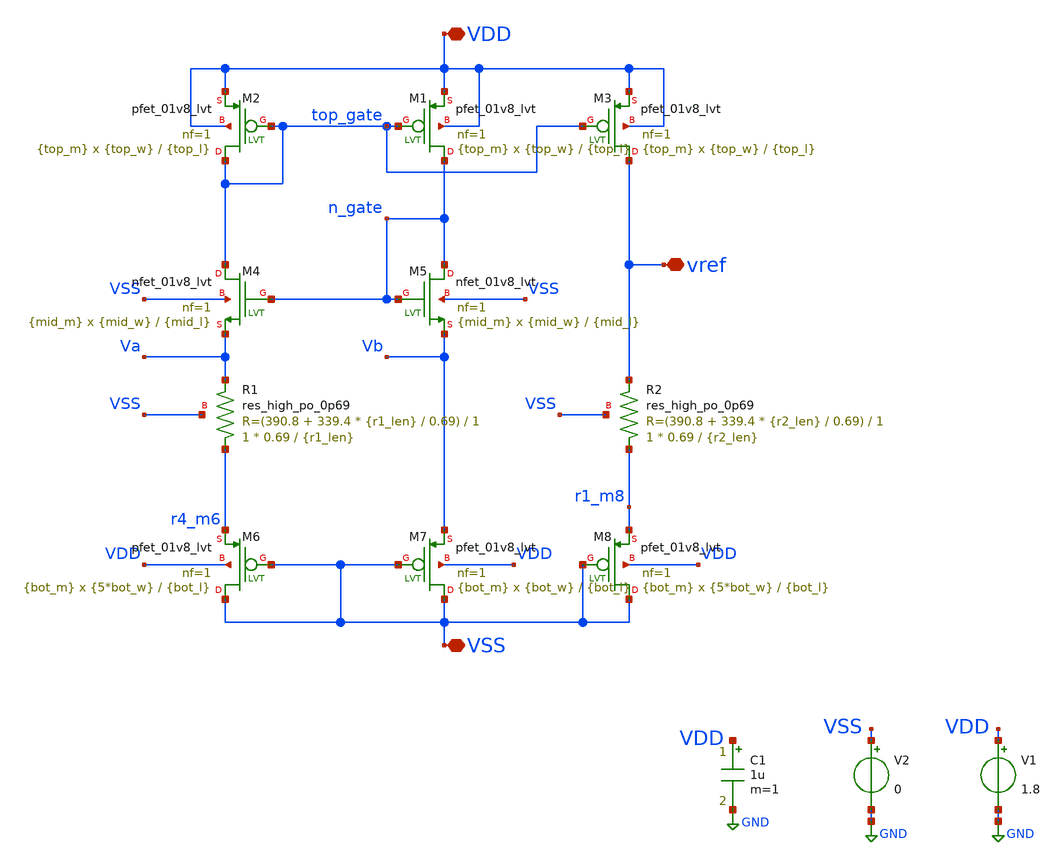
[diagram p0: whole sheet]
** sch_path: xschem/bandgap-op.sch
**.subckt bandgap-op VSS VDD vref
*.iopin VSS
*.iopin VDD
*.iopin vref
XR1 r4_m6 Va VSS sky130_fd_pr__res_high_po_0p69 L={r1_len} mult=1 m=1
XR2 r1_m8 vref VSS sky130_fd_pr__res_high_po_0p69 L={r2_len} mult=1 m=1
V1 VDD GND 1.8
V2 VSS GND 0
C1 VDD GND 1u m=1
XM5 n_gate n_gate Vb VSS sky130_fd_pr__nfet_01v8_lvt L={mid_l} W={mid_w} nf=1 ad='int((nf+1)/2) * W/nf * 0.29'
+ as='int((nf+2)/2) * W/nf * 0.29' pd='2*int((nf+1)/2) * (W/nf + 0.29)' ps='2*int((nf+2)/2) * (W/nf + 0.29)'
+ nrd='0.29 / W' nrs='0.29 / W' sa=0 sb=0 sd=0 mult={mid_m} m={mid_m}
XM3 vref top_gate VDD VDD sky130_fd_pr__pfet_01v8_lvt L={top_l} W={top_w} nf=1 ad='int((nf+1)/2) * W/nf * 0.29'
+ as='int((nf+2)/2) * W/nf * 0.29' pd='2*int((nf+1)/2) * (W/nf + 0.29)' ps='2*int((nf+2)/2) * (W/nf + 0.29)'
+ nrd='0.29 / W' nrs='0.29 / W' sa=0 sb=0 sd=0 mult={top_m} m={top_m}
XM1 n_gate top_gate VDD VDD sky130_fd_pr__pfet_01v8_lvt L={top_l} W={top_w} nf=1 ad='int((nf+1)/2) * W/nf * 0.29'
+ as='int((nf+2)/2) * W/nf * 0.29' pd='2*int((nf+1)/2) * (W/nf + 0.29)' ps='2*int((nf+2)/2) * (W/nf + 0.29)'
+ nrd='0.29 / W' nrs='0.29 / W' sa=0 sb=0 sd=0 mult={top_m} m={top_m}
XM2 top_gate top_gate VDD VDD sky130_fd_pr__pfet_01v8_lvt L={top_l} W={top_w} nf=1 ad='int((nf+1)/2) * W/nf * 0.29'
+ as='int((nf+2)/2) * W/nf * 0.29' pd='2*int((nf+1)/2) * (W/nf + 0.29)' ps='2*int((nf+2)/2) * (W/nf + 0.29)'
+ nrd='0.29 / W' nrs='0.29 / W' sa=0 sb=0 sd=0 mult={top_m} m={top_m}
XM4 top_gate n_gate Va VSS sky130_fd_pr__nfet_01v8_lvt L={mid_l} W={mid_w} nf=1 ad='int((nf+1)/2) * W/nf * 0.29'
+ as='int((nf+2)/2) * W/nf * 0.29' pd='2*int((nf+1)/2) * (W/nf + 0.29)' ps='2*int((nf+2)/2) * (W/nf + 0.29)'
+ nrd='0.29 / W' nrs='0.29 / W' sa=0 sb=0 sd=0 mult={mid_m} m={mid_m}
XM6 VSS VSS r4_m6 VDD sky130_fd_pr__pfet_01v8_lvt L={bot_l} W={5*bot_w} nf=1 ad='int((nf+1)/2) * W/nf * 0.29'
+ as='int((nf+2)/2) * W/nf * 0.29' pd='2*int((nf+1)/2) * (W/nf + 0.29)' ps='2*int((nf+2)/2) * (W/nf + 0.29)'
+ nrd='0.29 / W' nrs='0.29 / W' sa=0 sb=0 sd=0 mult={bot_m} m={bot_m}
XM8 VSS VSS r1_m8 VDD sky130_fd_pr__pfet_01v8_lvt L={bot_l} W={5*bot_w} nf=1 ad='int((nf+1)/2) * W/nf * 0.29'
+ as='int((nf+2)/2) * W/nf * 0.29' pd='2*int((nf+1)/2) * (W/nf + 0.29)' ps='2*int((nf+2)/2) * (W/nf + 0.29)'
+ nrd='0.29 / W' nrs='0.29 / W' sa=0 sb=0 sd=0 mult={bot_m} m={bot_m}
XM7 VSS VSS Vb VDD sky130_fd_pr__pfet_01v8_lvt L={bot_l} W={bot_w} nf=1 ad='int((nf+1)/2) * W/nf * 0.29'
+ as='int((nf+2)/2) * W/nf * 0.29' pd='2*int((nf+1)/2) * (W/nf + 0.29)' ps='2*int((nf+2)/2) * (W/nf + 0.29)'
+ nrd='0.29 / W' nrs='0.29 / W' sa=0 sb=0 sd=0 mult={bot_m} m={bot_m}
**** begin user architecture code

** opencircuitdesign pdks install
.lib $::SKYWATER_MODELS/sky130.lib.spice tt





.param top_l = 10
.param top_w = 20
.param top_m = 2

.param mid_l = 10
.param mid_w = 10
.param mid_m = 2

.param bot_l = 5
.param bot_w = 10
.param bot_m = 2
.param r1_len = 200
.param r2_len = 200
.control
*op
*write bandgap-op.raw
set appendwrite
*reset

*dc v1 1.3 2 0.01
*write bandgap-op.raw
*reset
let r1_len_val = 100
let r2_len_val = 100
repeat 10
  alterparam r2_len = $&r2_len_val
  let r2_len_val = r2_len_val + 50
  repeat 10
    alterparam r1_len = $&r1_len_val
    let r1_len_val = r1_len_val + 50
    dc temp 10 100 1
    write bandgap-op.raw
    reset
  end
end
*quit
.endc



**** end user architecture code
**.ends
.GLOBAL GND
.end
